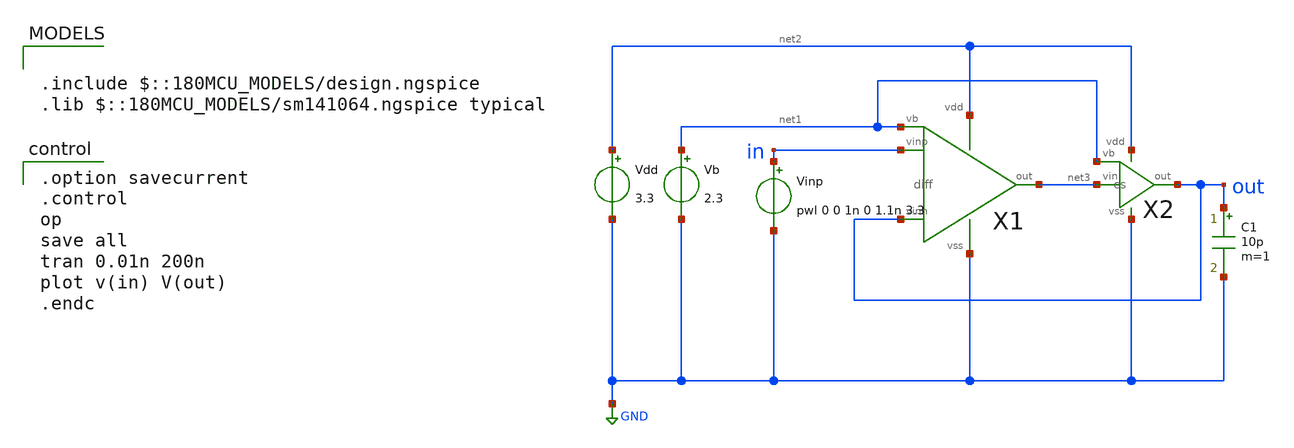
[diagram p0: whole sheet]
** sch_path: opamp/2stage_tran.sch
**.subckt 2stage_tran
Vdd net2 GND 3.3
Vb net1 GND 2.3
X1 in out net3 net2 GND net1 diff
X2 net3 net1 out net2 GND cs
C1 out GND 10p m=1
Vinp in GND pwl 0 0 1n 0 1.1n 3.3
**** begin user architecture code

.include $::180MCU_MODELS/design.ngspice
.lib $::180MCU_MODELS/sm141064.ngspice typical


.option savecurrent
.control
op
save all
tran 0.01n 200n
plot v(in) V(out)
.endc

**** end user architecture code
**.ends
.GLOBAL GND
.end
